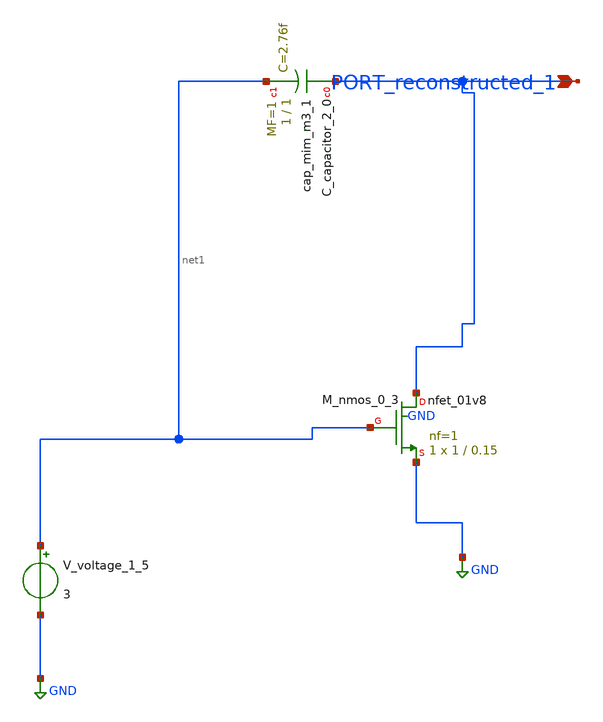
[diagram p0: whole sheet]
** sch_path: schematics/AMSNet/51.sch
**.subckt 51 PORT_reconstructed_1
*.ipin PORT_reconstructed_1
XC_capacitor_2_0 PORT_reconstructed_1 net1 sky130_fd_pr__cap_mim_m3_1 W=1 L=1 MF=1 m=1
XM_nmos_0_3 PORT_reconstructed_1 net1 GND GND sky130_fd_pr__nfet_01v8 L=0.15 W=1 nf=1 ad='int((1 + 1)/2) * 1 / 1 * 0.29'
+ as='int((1 + 2)/2) * 1 / 1 * 0.29' pd='2*int((1 + 1)/2) * (1 / 1 + 0.29)' ps='2*int((1 + 2)/2) * (1 / 1 + 0.29)'
+ nrd='0.29 / 1 ' nrs='0.29 / 1 ' sa=0 sb=0 sd=0 mult=1 m=1
V_voltage_1_5 net1 GND 3
**.ends
.GLOBAL GND
.end
